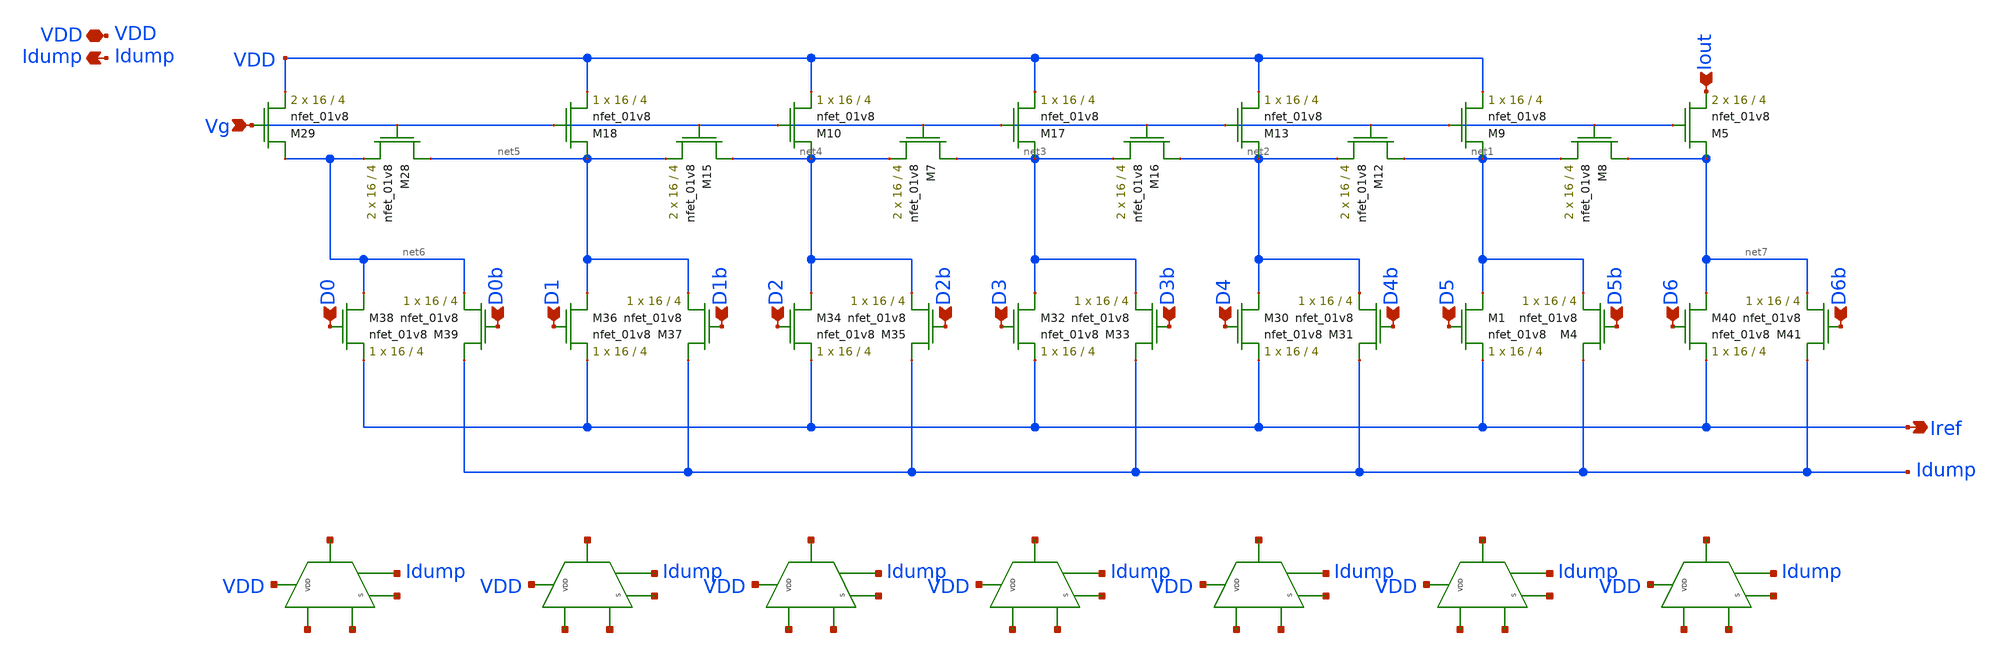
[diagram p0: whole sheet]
** sch_path: Final DAC files/schematics/DAC/MP4_DAC.sch
**.subckt MP4_DAC Iout Vg Iref Idump VDD D0 D1 D2 D3 D4 D5 D6 D0b D1b D2b D3b D4b D5b D6b
*.ipin Iout
*.ipin Vg
*.opin Iref
*.opin Idump
*.iopin VDD
*.ipin D0
*.ipin D1
*.ipin D2
*.ipin D3
*.ipin D4
*.ipin D5
*.ipin D6
*.ipin D0b
*.ipin D1b
*.ipin D2b
*.ipin D3b
*.ipin D4b
*.ipin D5b
*.ipin D6b
XM5 net7 Vg Iout GND sky130_fd_pr__nfet_01v8 L=4 W=16 nf=1 ad='int((nf+1)/2) * W/nf * 0.29' as='int((nf+2)/2) * W/nf * 0.29'
+ pd='2*int((nf+1)/2) * (W/nf + 0.29)' ps='2*int((nf+2)/2) * (W/nf + 0.29)' nrd='0.29 / W' nrs='0.29 / W'
+ sa=0 sb=0 sd=0 mult=2 m=2
XM8 net7 Vg net1 GND sky130_fd_pr__nfet_01v8 L=4 W=16 nf=1 ad='int((nf+1)/2) * W/nf * 0.29' as='int((nf+2)/2) * W/nf * 0.29'
+ pd='2*int((nf+1)/2) * (W/nf + 0.29)' ps='2*int((nf+2)/2) * (W/nf + 0.29)' nrd='0.29 / W' nrs='0.29 / W'
+ sa=0 sb=0 sd=0 mult=2 m=2
XM9 net1 Vg VDD GND sky130_fd_pr__nfet_01v8 L=4 W=16 nf=1 ad='int((nf+1)/2) * W/nf * 0.29' as='int((nf+2)/2) * W/nf * 0.29'
+ pd='2*int((nf+1)/2) * (W/nf + 0.29)' ps='2*int((nf+2)/2) * (W/nf + 0.29)' nrd='0.29 / W' nrs='0.29 / W'
+ sa=0 sb=0 sd=0 mult=1 m=1
XM12 net1 Vg net2 GND sky130_fd_pr__nfet_01v8 L=4 W=16 nf=1 ad='int((nf+1)/2) * W/nf * 0.29' as='int((nf+2)/2) * W/nf * 0.29'
+ pd='2*int((nf+1)/2) * (W/nf + 0.29)' ps='2*int((nf+2)/2) * (W/nf + 0.29)' nrd='0.29 / W' nrs='0.29 / W'
+ sa=0 sb=0 sd=0 mult=2 m=2
XM13 net2 Vg VDD GND sky130_fd_pr__nfet_01v8 L=4 W=16 nf=1 ad='int((nf+1)/2) * W/nf * 0.29' as='int((nf+2)/2) * W/nf * 0.29'
+ pd='2*int((nf+1)/2) * (W/nf + 0.29)' ps='2*int((nf+2)/2) * (W/nf + 0.29)' nrd='0.29 / W' nrs='0.29 / W'
+ sa=0 sb=0 sd=0 mult=1 m=1
XM16 net2 Vg net3 GND sky130_fd_pr__nfet_01v8 L=4 W=16 nf=1 ad='int((nf+1)/2) * W/nf * 0.29' as='int((nf+2)/2) * W/nf * 0.29'
+ pd='2*int((nf+1)/2) * (W/nf + 0.29)' ps='2*int((nf+2)/2) * (W/nf + 0.29)' nrd='0.29 / W' nrs='0.29 / W'
+ sa=0 sb=0 sd=0 mult=2 m=2
XM17 net3 Vg VDD GND sky130_fd_pr__nfet_01v8 L=4 W=16 nf=1 ad='int((nf+1)/2) * W/nf * 0.29' as='int((nf+2)/2) * W/nf * 0.29'
+ pd='2*int((nf+1)/2) * (W/nf + 0.29)' ps='2*int((nf+2)/2) * (W/nf + 0.29)' nrd='0.29 / W' nrs='0.29 / W'
+ sa=0 sb=0 sd=0 mult=1 m=1
XM7 net3 Vg net4 GND sky130_fd_pr__nfet_01v8 L=4 W=16 nf=1 ad='int((nf+1)/2) * W/nf * 0.29' as='int((nf+2)/2) * W/nf * 0.29'
+ pd='2*int((nf+1)/2) * (W/nf + 0.29)' ps='2*int((nf+2)/2) * (W/nf + 0.29)' nrd='0.29 / W' nrs='0.29 / W'
+ sa=0 sb=0 sd=0 mult=2 m=2
XM10 net4 Vg VDD GND sky130_fd_pr__nfet_01v8 L=4 W=16 nf=1 ad='int((nf+1)/2) * W/nf * 0.29' as='int((nf+2)/2) * W/nf * 0.29'
+ pd='2*int((nf+1)/2) * (W/nf + 0.29)' ps='2*int((nf+2)/2) * (W/nf + 0.29)' nrd='0.29 / W' nrs='0.29 / W'
+ sa=0 sb=0 sd=0 mult=1 m=1
XM15 net4 Vg net5 GND sky130_fd_pr__nfet_01v8 L=4 W=16 nf=1 ad='int((nf+1)/2) * W/nf * 0.29' as='int((nf+2)/2) * W/nf * 0.29'
+ pd='2*int((nf+1)/2) * (W/nf + 0.29)' ps='2*int((nf+2)/2) * (W/nf + 0.29)' nrd='0.29 / W' nrs='0.29 / W'
+ sa=0 sb=0 sd=0 mult=2 m=2
XM18 net5 Vg VDD GND sky130_fd_pr__nfet_01v8 L=4 W=16 nf=1 ad='int((nf+1)/2) * W/nf * 0.29' as='int((nf+2)/2) * W/nf * 0.29'
+ pd='2*int((nf+1)/2) * (W/nf + 0.29)' ps='2*int((nf+2)/2) * (W/nf + 0.29)' nrd='0.29 / W' nrs='0.29 / W'
+ sa=0 sb=0 sd=0 mult=1 m=1
XM28 net5 Vg net6 GND sky130_fd_pr__nfet_01v8 L=4 W=16 nf=1 ad='int((nf+1)/2) * W/nf * 0.29' as='int((nf+2)/2) * W/nf * 0.29'
+ pd='2*int((nf+1)/2) * (W/nf + 0.29)' ps='2*int((nf+2)/2) * (W/nf + 0.29)' nrd='0.29 / W' nrs='0.29 / W'
+ sa=0 sb=0 sd=0 mult=2 m=2
XM29 net6 Vg VDD GND sky130_fd_pr__nfet_01v8 L=4 W=16 nf=1 ad='int((nf+1)/2) * W/nf * 0.29' as='int((nf+2)/2) * W/nf * 0.29'
+ pd='2*int((nf+1)/2) * (W/nf + 0.29)' ps='2*int((nf+2)/2) * (W/nf + 0.29)' nrd='0.29 / W' nrs='0.29 / W'
+ sa=0 sb=0 sd=0 mult=2 m=2
XM1 net1 D5 Iref GND sky130_fd_pr__nfet_01v8 L=4 W=16 nf=1 ad='int((nf+1)/2) * W/nf * 0.29' as='int((nf+2)/2) * W/nf * 0.29'
+ pd='2*int((nf+1)/2) * (W/nf + 0.29)' ps='2*int((nf+2)/2) * (W/nf + 0.29)' nrd='0.29 / W' nrs='0.29 / W'
+ sa=0 sb=0 sd=0 mult=1 m=1
XM4 Idump D5b net1 GND sky130_fd_pr__nfet_01v8 L=4 W=16 nf=1 ad='int((nf+1)/2) * W/nf * 0.29' as='int((nf+2)/2) * W/nf * 0.29'
+ pd='2*int((nf+1)/2) * (W/nf + 0.29)' ps='2*int((nf+2)/2) * (W/nf + 0.29)' nrd='0.29 / W' nrs='0.29 / W'
+ sa=0 sb=0 sd=0 mult=1 m=1
XM30 net2 D4 Iref GND sky130_fd_pr__nfet_01v8 L=4 W=16 nf=1 ad='int((nf+1)/2) * W/nf * 0.29' as='int((nf+2)/2) * W/nf * 0.29'
+ pd='2*int((nf+1)/2) * (W/nf + 0.29)' ps='2*int((nf+2)/2) * (W/nf + 0.29)' nrd='0.29 / W' nrs='0.29 / W'
+ sa=0 sb=0 sd=0 mult=1 m=1
XM31 Idump D4b net2 GND sky130_fd_pr__nfet_01v8 L=4 W=16 nf=1 ad='int((nf+1)/2) * W/nf * 0.29' as='int((nf+2)/2) * W/nf * 0.29'
+ pd='2*int((nf+1)/2) * (W/nf + 0.29)' ps='2*int((nf+2)/2) * (W/nf + 0.29)' nrd='0.29 / W' nrs='0.29 / W'
+ sa=0 sb=0 sd=0 mult=1 m=1
XM32 net3 D3 Iref GND sky130_fd_pr__nfet_01v8 L=4 W=16 nf=1 ad='int((nf+1)/2) * W/nf * 0.29' as='int((nf+2)/2) * W/nf * 0.29'
+ pd='2*int((nf+1)/2) * (W/nf + 0.29)' ps='2*int((nf+2)/2) * (W/nf + 0.29)' nrd='0.29 / W' nrs='0.29 / W'
+ sa=0 sb=0 sd=0 mult=1 m=1
XM33 Idump D3b net3 GND sky130_fd_pr__nfet_01v8 L=4 W=16 nf=1 ad='int((nf+1)/2) * W/nf * 0.29' as='int((nf+2)/2) * W/nf * 0.29'
+ pd='2*int((nf+1)/2) * (W/nf + 0.29)' ps='2*int((nf+2)/2) * (W/nf + 0.29)' nrd='0.29 / W' nrs='0.29 / W'
+ sa=0 sb=0 sd=0 mult=1 m=1
XM34 net4 D2 Iref GND sky130_fd_pr__nfet_01v8 L=4 W=16 nf=1 ad='int((nf+1)/2) * W/nf * 0.29' as='int((nf+2)/2) * W/nf * 0.29'
+ pd='2*int((nf+1)/2) * (W/nf + 0.29)' ps='2*int((nf+2)/2) * (W/nf + 0.29)' nrd='0.29 / W' nrs='0.29 / W'
+ sa=0 sb=0 sd=0 mult=1 m=1
XM35 Idump D2b net4 GND sky130_fd_pr__nfet_01v8 L=4 W=16 nf=1 ad='int((nf+1)/2) * W/nf * 0.29' as='int((nf+2)/2) * W/nf * 0.29'
+ pd='2*int((nf+1)/2) * (W/nf + 0.29)' ps='2*int((nf+2)/2) * (W/nf + 0.29)' nrd='0.29 / W' nrs='0.29 / W'
+ sa=0 sb=0 sd=0 mult=1 m=1
XM36 net5 D1 Iref GND sky130_fd_pr__nfet_01v8 L=4 W=16 nf=1 ad='int((nf+1)/2) * W/nf * 0.29' as='int((nf+2)/2) * W/nf * 0.29'
+ pd='2*int((nf+1)/2) * (W/nf + 0.29)' ps='2*int((nf+2)/2) * (W/nf + 0.29)' nrd='0.29 / W' nrs='0.29 / W'
+ sa=0 sb=0 sd=0 mult=1 m=1
XM37 Idump D1b net5 GND sky130_fd_pr__nfet_01v8 L=4 W=16 nf=1 ad='int((nf+1)/2) * W/nf * 0.29' as='int((nf+2)/2) * W/nf * 0.29'
+ pd='2*int((nf+1)/2) * (W/nf + 0.29)' ps='2*int((nf+2)/2) * (W/nf + 0.29)' nrd='0.29 / W' nrs='0.29 / W'
+ sa=0 sb=0 sd=0 mult=1 m=1
XM38 net6 D0 Iref GND sky130_fd_pr__nfet_01v8 L=4 W=16 nf=1 ad='int((nf+1)/2) * W/nf * 0.29' as='int((nf+2)/2) * W/nf * 0.29'
+ pd='2*int((nf+1)/2) * (W/nf + 0.29)' ps='2*int((nf+2)/2) * (W/nf + 0.29)' nrd='0.29 / W' nrs='0.29 / W'
+ sa=0 sb=0 sd=0 mult=1 m=1
XM39 Idump D0b net6 GND sky130_fd_pr__nfet_01v8 L=4 W=16 nf=1 ad='int((nf+1)/2) * W/nf * 0.29' as='int((nf+2)/2) * W/nf * 0.29'
+ pd='2*int((nf+1)/2) * (W/nf + 0.29)' ps='2*int((nf+2)/2) * (W/nf + 0.29)' nrd='0.29 / W' nrs='0.29 / W'
+ sa=0 sb=0 sd=0 mult=1 m=1
XM40 net7 D6 Iref GND sky130_fd_pr__nfet_01v8 L=4 W=16 nf=1 ad='int((nf+1)/2) * W/nf * 0.29' as='int((nf+2)/2) * W/nf * 0.29'
+ pd='2*int((nf+1)/2) * (W/nf + 0.29)' ps='2*int((nf+2)/2) * (W/nf + 0.29)' nrd='0.29 / W' nrs='0.29 / W'
+ sa=0 sb=0 sd=0 mult=1 m=1
XM41 Idump D6b net7 GND sky130_fd_pr__nfet_01v8 L=4 W=16 nf=1 ad='int((nf+1)/2) * W/nf * 0.29' as='int((nf+2)/2) * W/nf * 0.29'
+ pd='2*int((nf+1)/2) * (W/nf + 0.29)' ps='2*int((nf+2)/2) * (W/nf + 0.29)' nrd='0.29 / W' nrs='0.29 / W'
+ sa=0 sb=0 sd=0 mult=1 m=1
**.ends
.end
